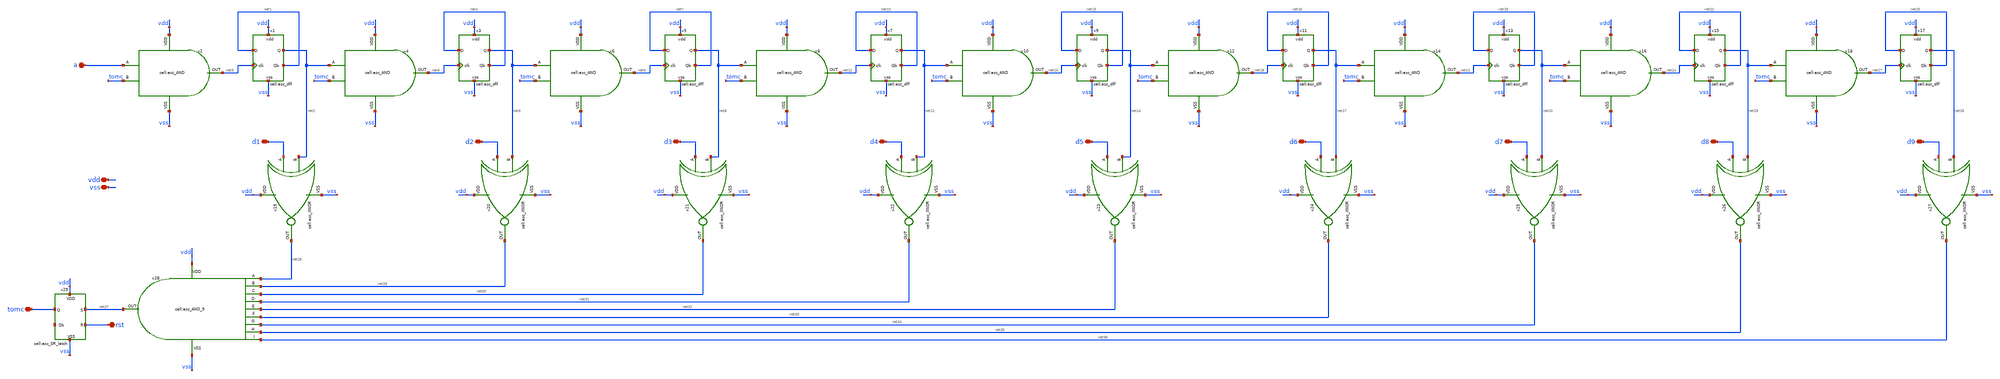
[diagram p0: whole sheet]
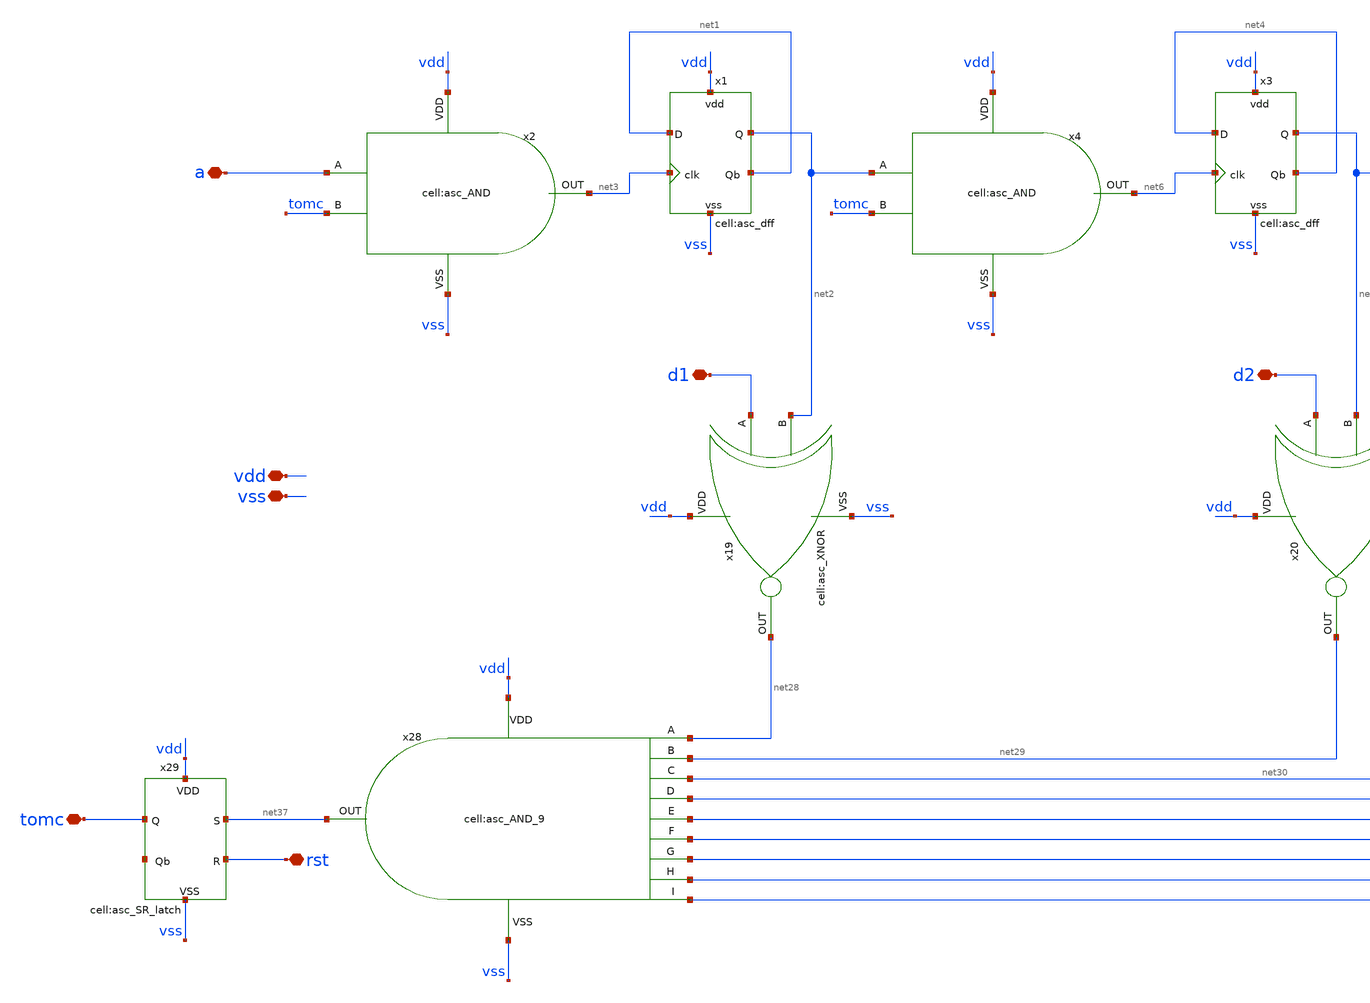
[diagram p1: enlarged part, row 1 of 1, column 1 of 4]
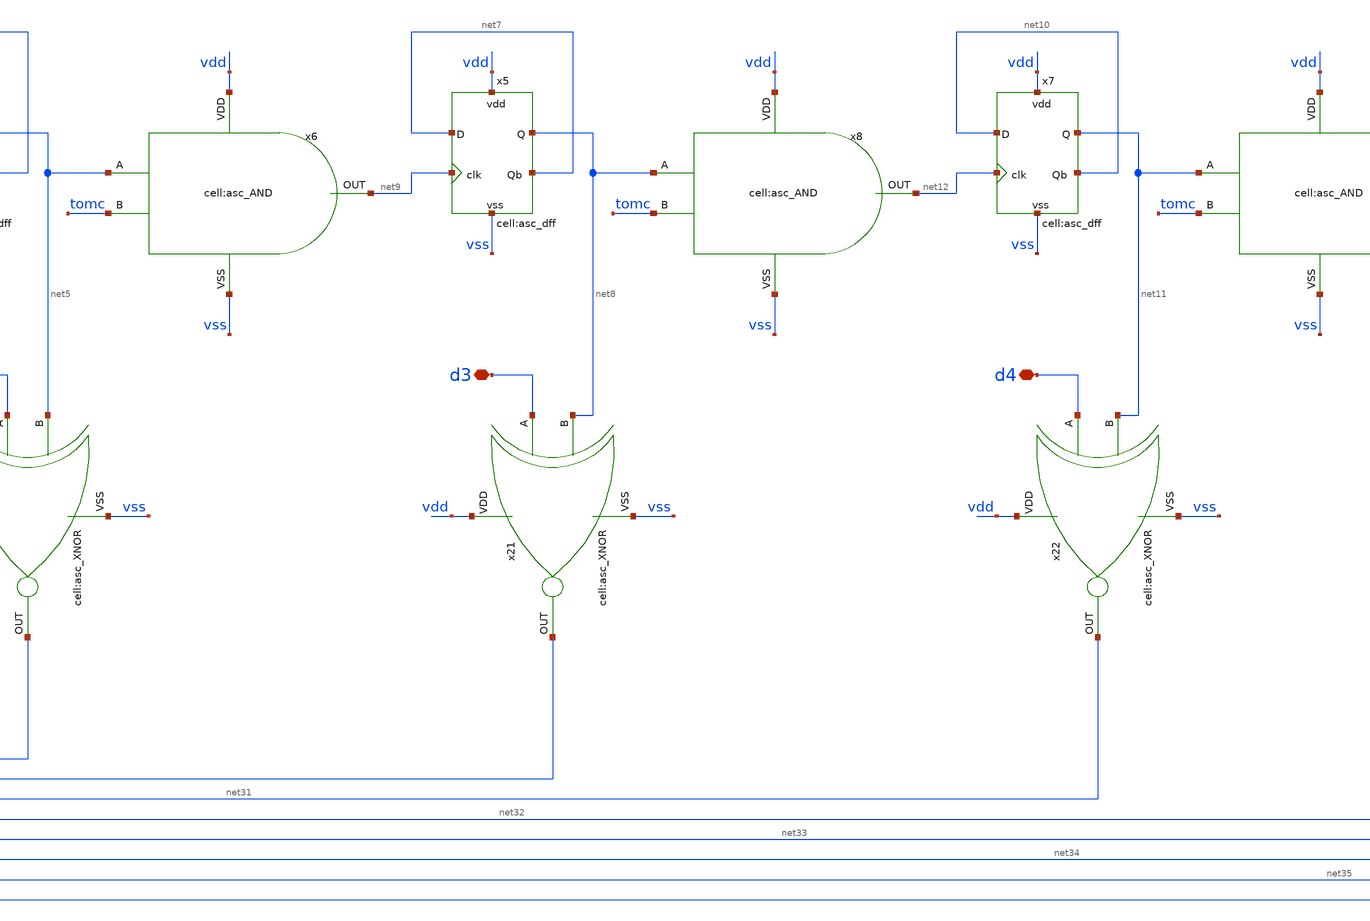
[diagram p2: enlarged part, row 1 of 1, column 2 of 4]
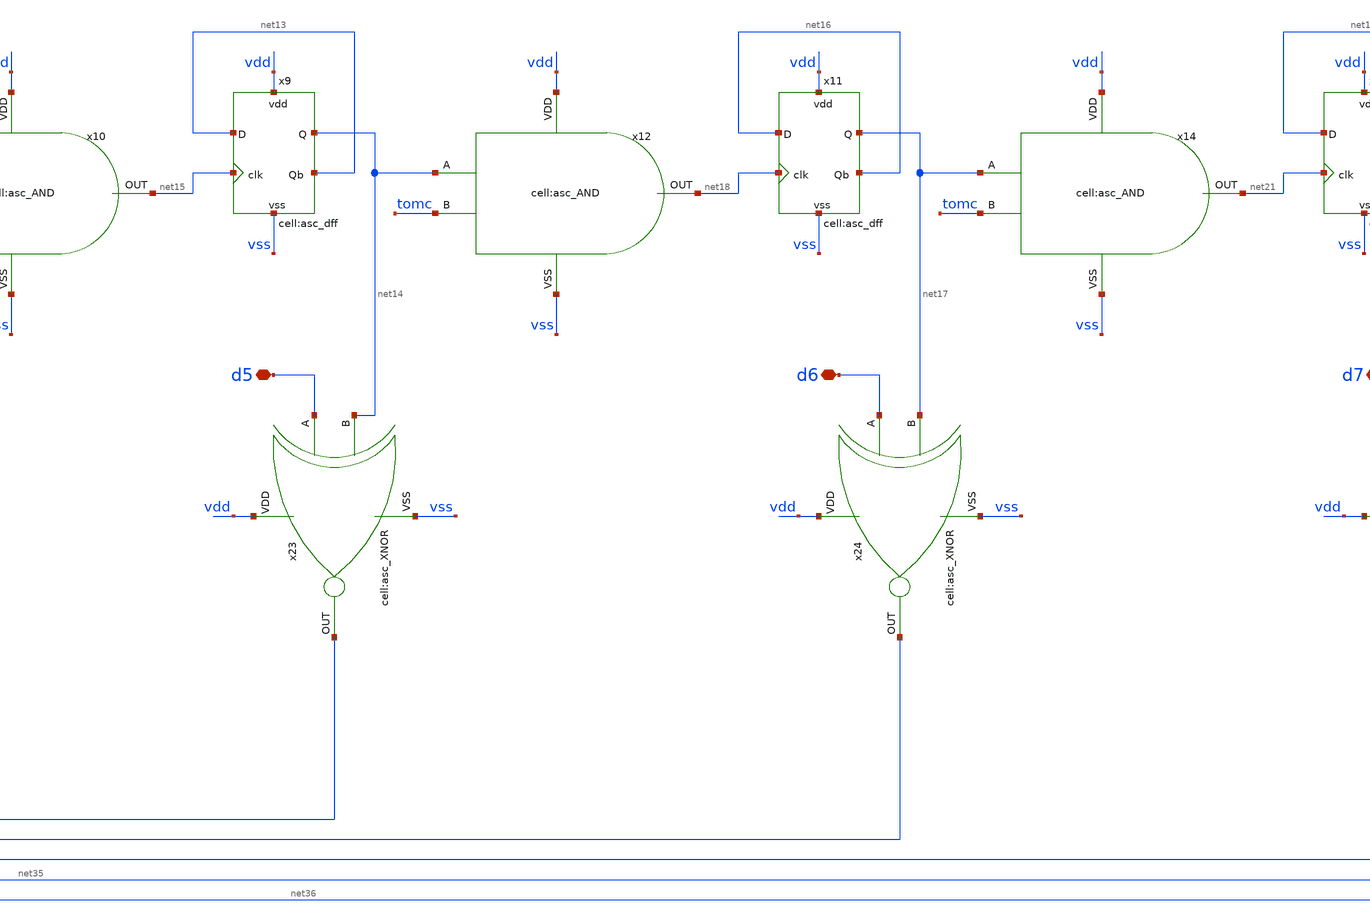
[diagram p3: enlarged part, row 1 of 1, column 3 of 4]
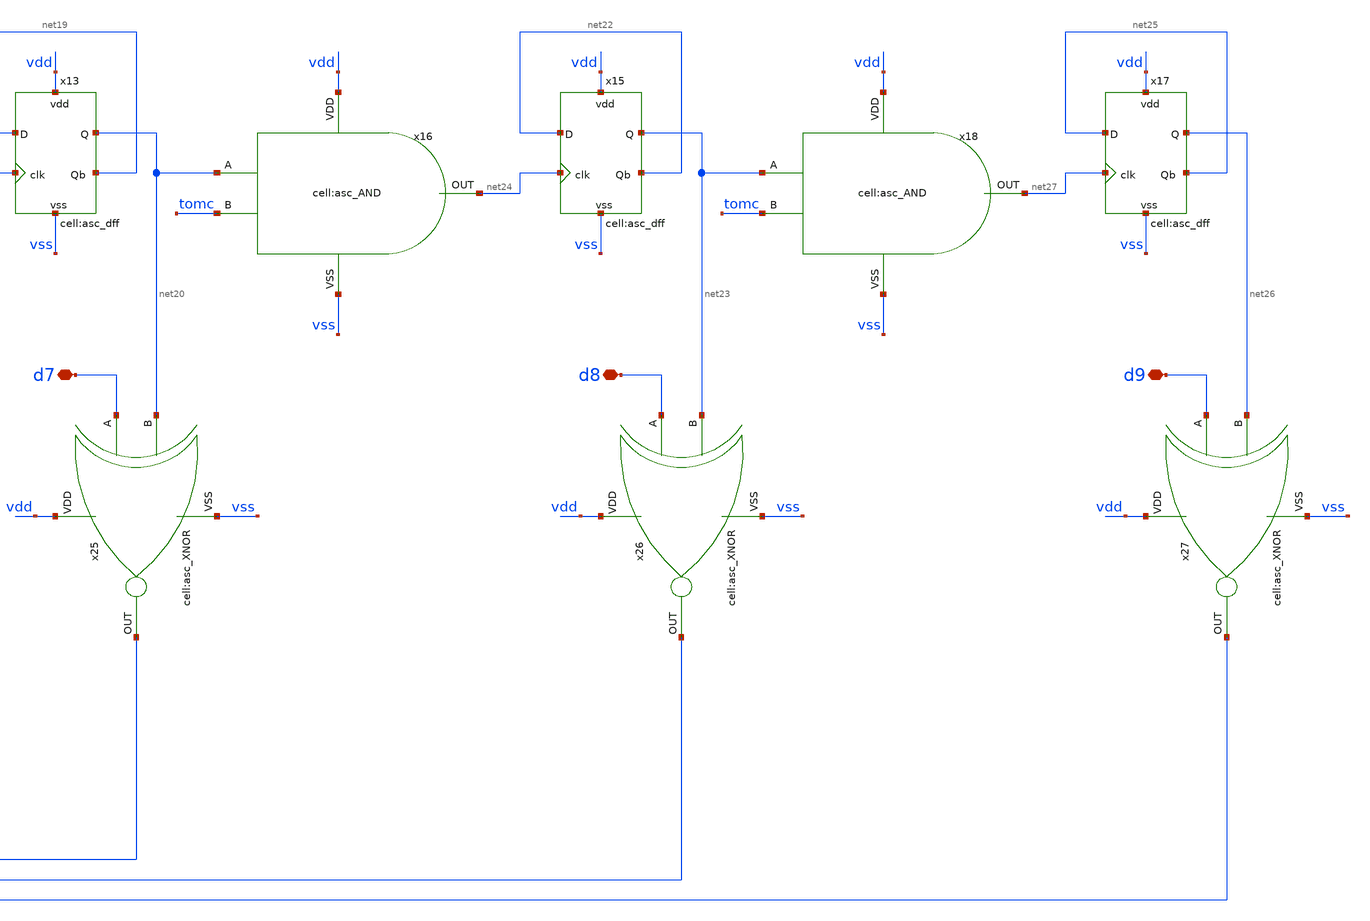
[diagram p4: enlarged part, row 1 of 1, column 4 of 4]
** sch_path: designs/libs/core_analog/asc_swallow_counter/asc_swallow_counter.sch
**.subckt asc_swallow_counter a vdd vss tomc d1 d2 d3 d4 d5 d6 d7 d8 d9 rst
*.iopin a
*.iopin vdd
*.iopin vss
*.iopin tomc
*.iopin d1
*.iopin d2
*.iopin d3
*.iopin d4
*.iopin d5
*.iopin d6
*.iopin d7
*.iopin d8
*.iopin d9
*.iopin rst
x1 net3 net1 net1 vdd vss net2 asc_dff
x2 vdd net3 a tomc vss asc_AND
x3 net6 net4 net4 vdd vss net5 asc_dff
x4 vdd net6 net2 tomc vss asc_AND
x5 net9 net7 net7 vdd vss net8 asc_dff
x6 vdd net9 net5 tomc vss asc_AND
x7 net12 net10 net10 vdd vss net11 asc_dff
x8 vdd net12 net8 tomc vss asc_AND
x9 net15 net13 net13 vdd vss net14 asc_dff
x10 vdd net15 net11 tomc vss asc_AND
x11 net18 net16 net16 vdd vss net17 asc_dff
x12 vdd net18 net14 tomc vss asc_AND
x13 net21 net19 net19 vdd vss net20 asc_dff
x14 vdd net21 net17 tomc vss asc_AND
x15 net24 net22 net22 vdd vss net23 asc_dff
x16 vdd net24 net20 tomc vss asc_AND
x17 net27 net25 net25 vdd vss net26 asc_dff
x18 vdd net27 net23 tomc vss asc_AND
x19 vdd vss net28 d1 net2 asc_XNOR
x20 vdd vss net29 d2 net5 asc_XNOR
x21 vdd vss net30 d3 net8 asc_XNOR
x22 vdd vss net31 d4 net11 asc_XNOR
x23 vdd vss net32 d5 net14 asc_XNOR
x24 vdd vss net33 d6 net17 asc_XNOR
x25 vdd vss net34 d7 net20 asc_XNOR
x26 vdd vss net35 d8 net23 asc_XNOR
x27 vdd vss net36 d9 net26 asc_XNOR
x28 vdd vss net37 net28 net29 net30 net31 net32 net33 net34 net35 net36 asc_AND_9
x29 rst net37 net38 vdd vss tomc asc_SR_latch
**.ends
.end
